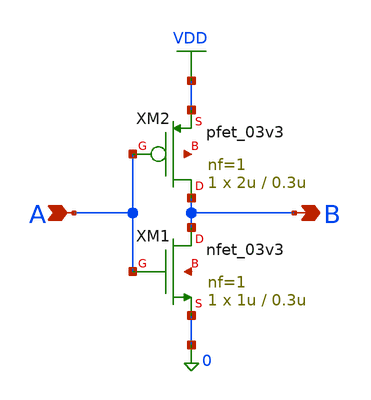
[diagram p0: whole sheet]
** sch_path: Chandra/inv4switch.sch
**.subckt inv4switch A B
*.ipin A
*.opin B
XM1 B A 0 net1 nfet_03v3 L=0.3u W=1u nf=1 ad='int((nf+1)/2) * W/nf * 0.18u' as='int((nf+2)/2) * W/nf * 0.18u'
+ pd='2*int((nf+1)/2) * (W/nf + 0.18u)' ps='2*int((nf+2)/2) * (W/nf + 0.18u)' nrd='0.18u / W' nrs='0.18u / W'
+ sa=0 sb=0 sd=0 m=1
XM2 B A VDD net2 pfet_03v3 L=0.3u W=2u nf=1 ad='int((nf+1)/2) * W/nf * 0.18u' as='int((nf+2)/2) * W/nf * 0.18u'
+ pd='2*int((nf+1)/2) * (W/nf + 0.18u)' ps='2*int((nf+2)/2) * (W/nf + 0.18u)' nrd='0.18u / W' nrs='0.18u / W'
+ sa=0 sb=0 sd=0 m=1
**.ends
.GLOBAL VDD
.end
